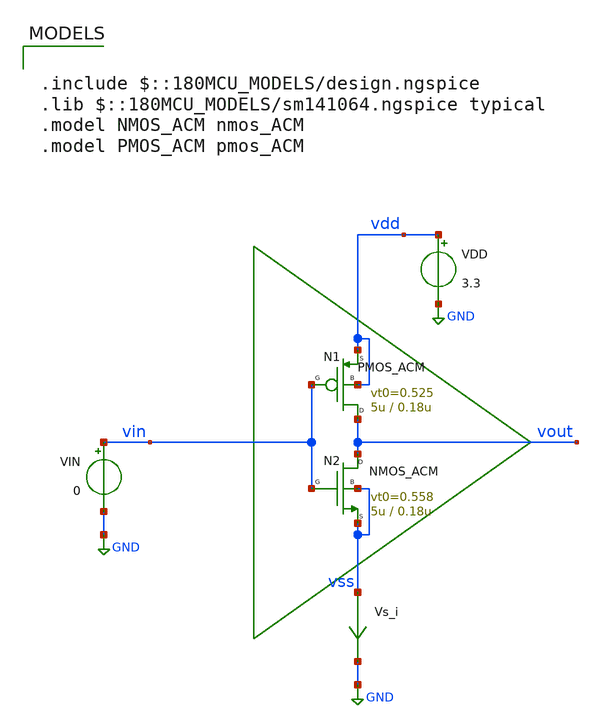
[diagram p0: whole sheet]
** sch_path: gf_tutorials/ACM/TB_inv_acm_vt0.sch
**.subckt TB_inv_acm_vt0
VIN vin GND 0
VDD vdd GND 3.3
Vs_i vss GND 0
.save i(vs_i)
N2 vout vin vss vss NMOS_ACM w=5u l=0.18u n=1.37 is=5.52u vt0=0.558 sigma=27m zeta=56m
N1 vout vin vdd vdd PMOS_ACM w=5u l=0.18u n=1.40 is=1.82u vt0=0.525 sigma=24m zeta=35m
**** begin user architecture code

.include $::180MCU_MODELS/design.ngspice
.lib $::180MCU_MODELS/sm141064.ngspice typical
.model NMOS_ACM nmos_ACM
.model PMOS_ACM pmos_ACM



.option gmin=1e-18
.control
pre_osdi /home/gmaranhao/Desktop/gf180_work/ACM/NMOS_ACM_2V0.osdi
pre_osdi /home/gmaranhao/Desktop/gf180_work/ACM/PMOS_ACM_2V0.osdi
save all

op
remzerovec
write TB_inv_acm_vt0.raw
set appendwrite

dc VIN 0 3.3 1m
remzerovec
write TB_inv_acm_vt0.raw
set appendwrite

.endc


**** end user architecture code
**.ends
.GLOBAL GND
.end
